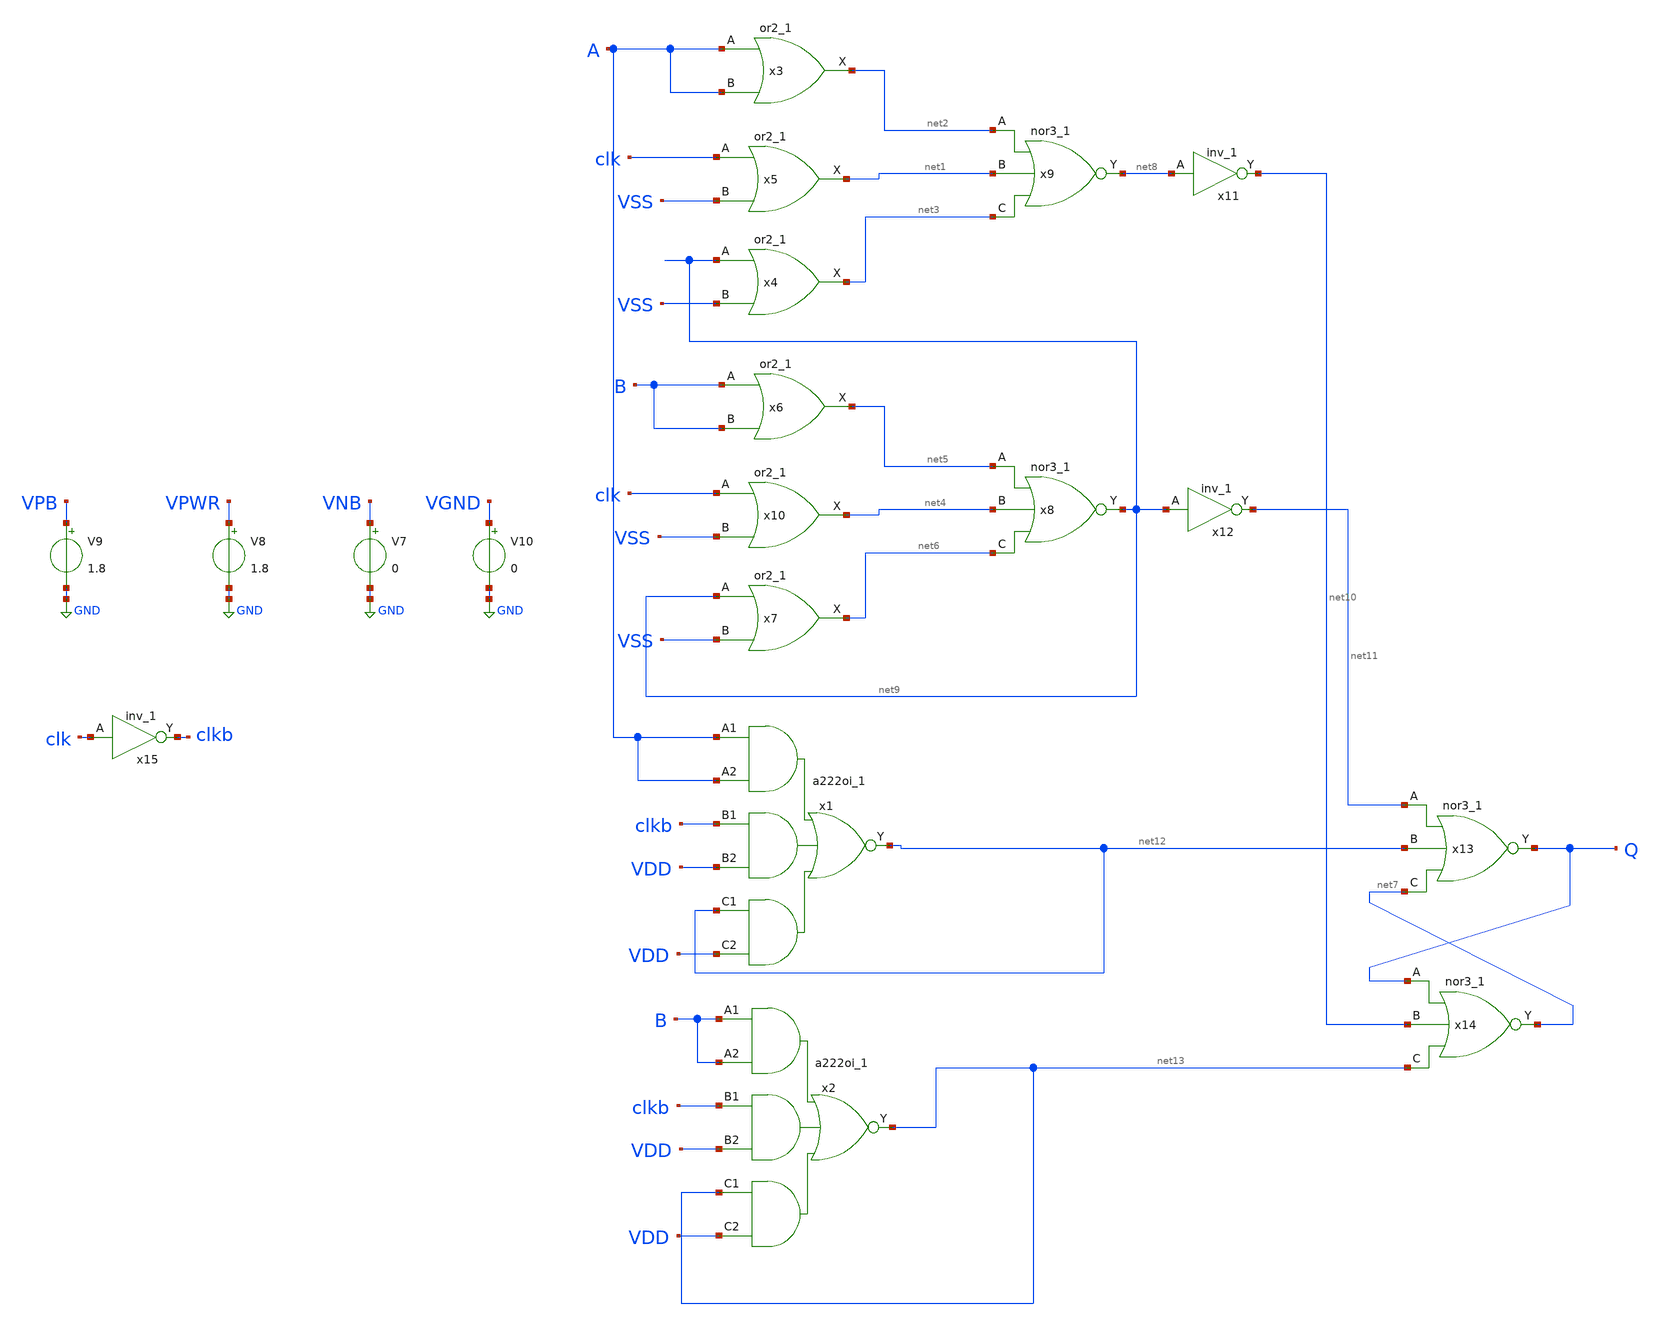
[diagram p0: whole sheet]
** sch_path: cmp/cmpoaisch.sch
**.subckt cmpoaisch
x1 A A clkb VDD net12 VDD VGND VNB VPB VPWR net12 sky130_fd_sc_hd__a222oi_1
x2 B B clkb VDD net13 VDD VGND VNB VPB VPWR net13 sky130_fd_sc_hd__a222oi_1
x3 A A VGND VNB VPB VPWR net2 sky130_fd_sc_hd__or2_1
x4 net9 VSS VGND VNB VPB VPWR net3 sky130_fd_sc_hd__or2_1
x9 net2 net1 net3 VGND VNB VPB VPWR net8 sky130_fd_sc_hd__nor3_1
x5 clk VSS VGND VNB VPB VPWR net1 sky130_fd_sc_hd__or2_1
x6 B B VGND VNB VPB VPWR net5 sky130_fd_sc_hd__or2_1
x7 net9 VSS VGND VNB VPB VPWR net6 sky130_fd_sc_hd__or2_1
x8 net5 net4 net6 VGND VNB VPB VPWR net9 sky130_fd_sc_hd__nor3_1
x10 clk VSS VGND VNB VPB VPWR net4 sky130_fd_sc_hd__or2_1
x11 net8 VGND VNB VPB VPWR net10 sky130_fd_sc_hd__inv_1
x12 net9 VGND VNB VPB VPWR net11 sky130_fd_sc_hd__inv_1
x13 net11 net12 net7 VGND VNB VPB VPWR Q sky130_fd_sc_hd__nor3_1
x14 Q net10 net13 VGND VNB VPB VPWR net7 sky130_fd_sc_hd__nor3_1
V7 VNB GND 0
V8 VPWR GND 1.8
V9 VPB GND 1.8
V10 VGND GND 0
x15 clk VGND VNB VPB VPWR clkb sky130_fd_sc_hd__inv_1
**.ends
.GLOBAL GND
.end
